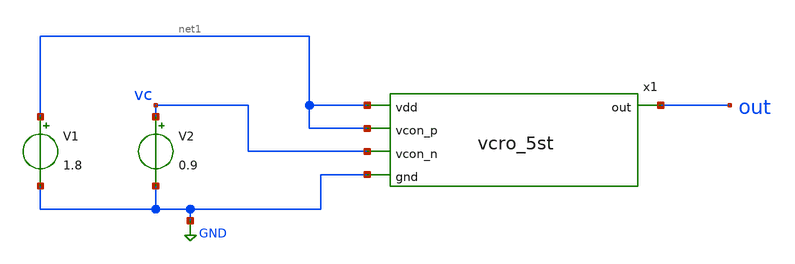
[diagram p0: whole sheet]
** sch_path: xschem/untitled-1.sch
**.subckt untitled-1
x1 net1 net1 out vc GND vcro_5st
V1 net1 GND 1.8
V2 vc GND 0.9
**** begin user architecture code
 .lib $::SKYWATER_MODELS/sky130.lib.spice tt

.param mc_mm_switch=0
.param mc_pr_switch=1



.option wnflag=0
.option savecurrents
.control
save all
tran 10n 2u
plot vc out
write vcro5.raw
op
.endc


**** end user architecture code
**.ends
.GLOBAL GND
.end
